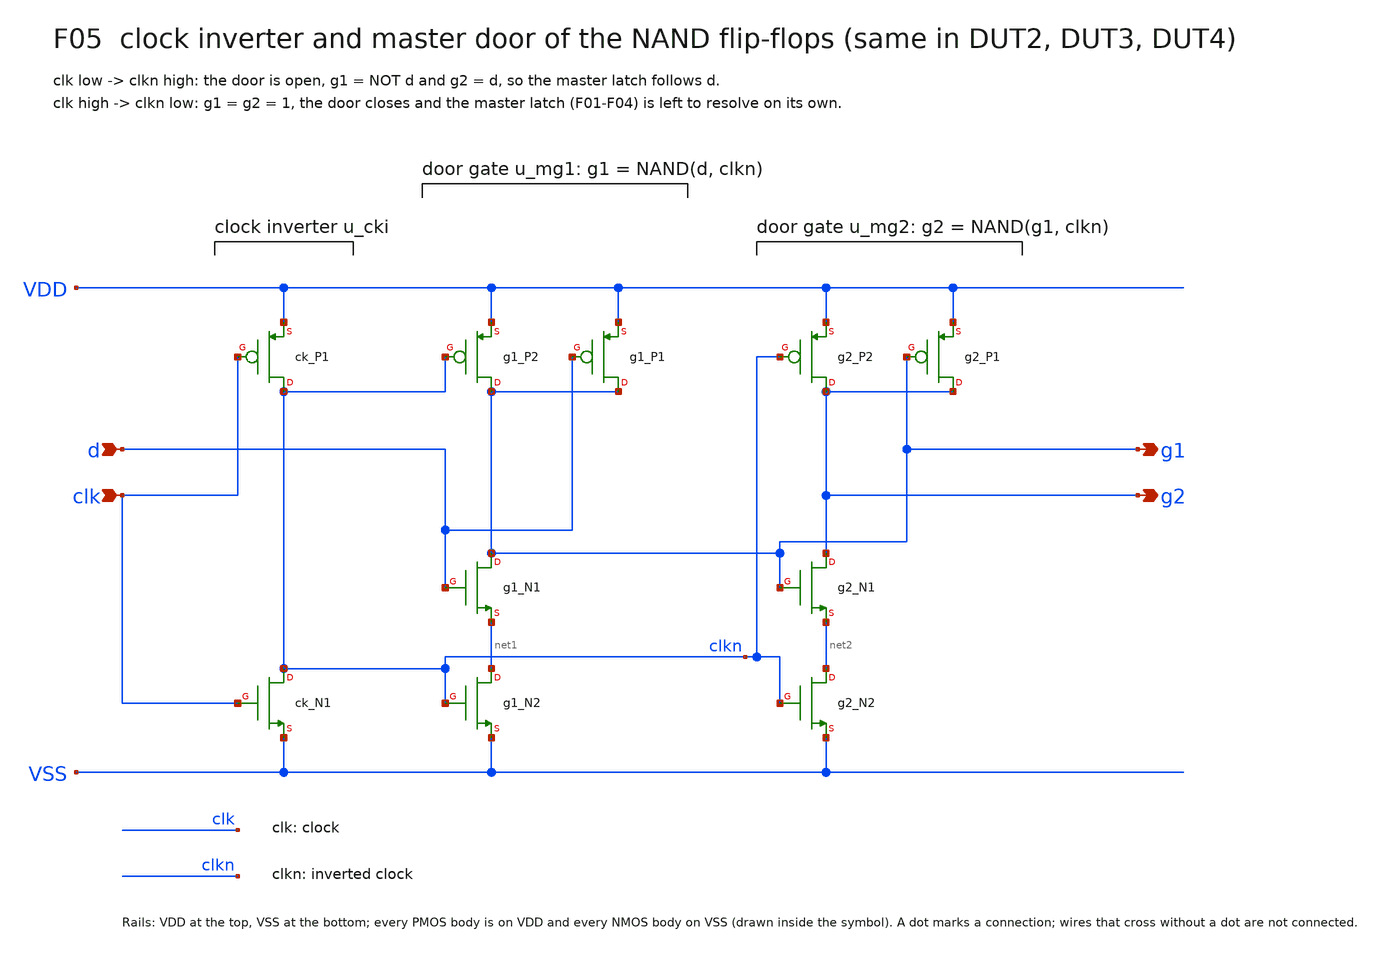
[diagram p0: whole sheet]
** sch_path: xschem/focus/F05_master_door.sch
**.subckt F05_master_door d clk g1 g2
*.ipin d
*.ipin clk
*.opin g1
*.opin g2
Xck_N1 clkn clk VSS VSS nfet_05v0 L=0.6u W=0.82u nf=1 m=1
Xck_P1 clkn clk VDD VDD pfet_05v0 L=0.5u W=1.22u nf=1 m=1
Xg1_N2 net1 clkn VSS VSS nfet_05v0 L=0.6u W=0.82u nf=1 m=1
Xg1_N1 g1 d net1 VSS nfet_05v0 L=0.6u W=0.82u nf=1 m=1
Xg1_P2 g1 clkn VDD VDD pfet_05v0 L=0.5u W=1.13u nf=1 m=1
Xg1_P1 g1 d VDD VDD pfet_05v0 L=0.5u W=1.13u nf=1 m=1
Xg2_N2 net2 clkn VSS VSS nfet_05v0 L=0.6u W=0.82u nf=1 m=1
Xg2_N1 g2 g1 net2 VSS nfet_05v0 L=0.6u W=0.82u nf=1 m=1
Xg2_P2 g2 clkn VDD VDD pfet_05v0 L=0.5u W=1.13u nf=1 m=1
Xg2_P1 g2 g1 VDD VDD pfet_05v0 L=0.5u W=1.13u nf=1 m=1
**.ends
.end
